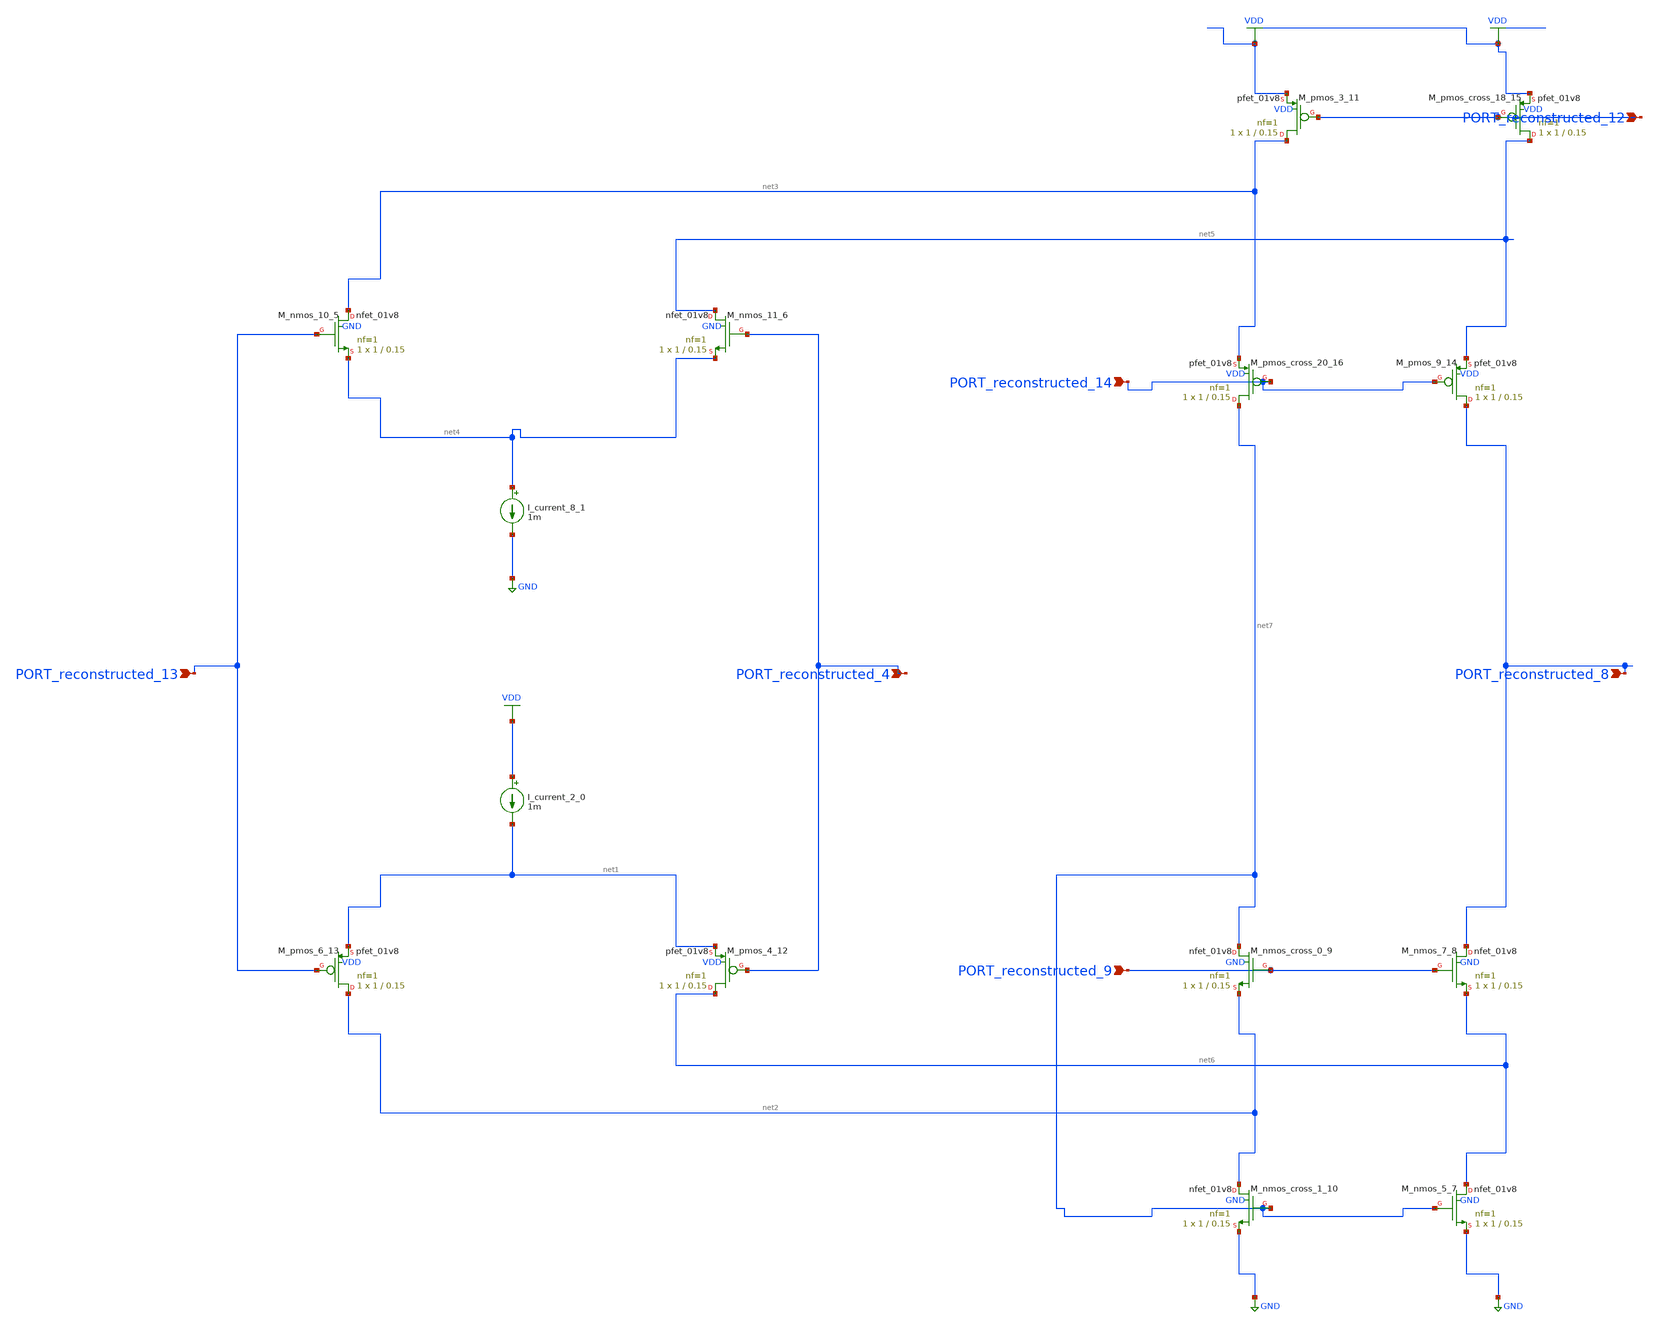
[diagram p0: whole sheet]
** sch_path: schematics/AMSNet/684.sch
**.subckt 684 PORT_reconstructed_4 PORT_reconstructed_8 PORT_reconstructed_13 PORT_reconstructed_9
*+ PORT_reconstructed_14 PORT_reconstructed_12
*.ipin PORT_reconstructed_4
*.ipin PORT_reconstructed_8
*.ipin PORT_reconstructed_13
*.ipin PORT_reconstructed_9
*.ipin PORT_reconstructed_14
*.ipin PORT_reconstructed_12
I_current_2_0 VDD net1 1m
I_current_8_1 net4 GND 1m
XM_nmos_10_5 net3 PORT_reconstructed_13 net4 GND sky130_fd_pr__nfet_01v8 L=0.15 W=1 nf=1 ad='int((1 + 1)/2) * 1 / 1 * 0.29'
+ as='int((1 + 2)/2) * 1 / 1 * 0.29' pd='2*int((1 + 1)/2) * (1 / 1 + 0.29)' ps='2*int((1 + 2)/2) * (1 / 1 + 0.29)'
+ nrd='0.29 / 1 ' nrs='0.29 / 1 ' sa=0 sb=0 sd=0 mult=1 m=1
XM_nmos_11_6 net5 PORT_reconstructed_4 net4 GND sky130_fd_pr__nfet_01v8 L=0.15 W=1 nf=1 ad='int((1 + 1)/2) * 1 / 1 * 0.29'
+ as='int((1 + 2)/2) * 1 / 1 * 0.29' pd='2*int((1 + 1)/2) * (1 / 1 + 0.29)' ps='2*int((1 + 2)/2) * (1 / 1 + 0.29)'
+ nrd='0.29 / 1 ' nrs='0.29 / 1 ' sa=0 sb=0 sd=0 mult=1 m=1
XM_nmos_5_7 net6 net7 GND GND sky130_fd_pr__nfet_01v8 L=0.15 W=1 nf=1 ad='int((1 + 1)/2) * 1 / 1 * 0.29'
+ as='int((1 + 2)/2) * 1 / 1 * 0.29' pd='2*int((1 + 1)/2) * (1 / 1 + 0.29)' ps='2*int((1 + 2)/2) * (1 / 1 + 0.29)'
+ nrd='0.29 / 1 ' nrs='0.29 / 1 ' sa=0 sb=0 sd=0 mult=1 m=1
XM_nmos_7_8 PORT_reconstructed_8 PORT_reconstructed_9 net6 GND sky130_fd_pr__nfet_01v8 L=0.15 W=1 nf=1
+ ad='int((1 + 1)/2) * 1 / 1 * 0.29' as='int((1 + 2)/2) * 1 / 1 * 0.29' pd='2*int((1 + 1)/2) * (1 / 1 + 0.29)'
+ ps='2*int((1 + 2)/2) * (1 / 1 + 0.29)' nrd='0.29 / 1 ' nrs='0.29 / 1 ' sa=0 sb=0 sd=0 mult=1 m=1
XM_nmos_cross_0_9 net7 PORT_reconstructed_9 net2 GND sky130_fd_pr__nfet_01v8 L=0.15 W=1 nf=1 ad='int((1 + 1)/2) * 1 / 1 * 0.29'
+ as='int((1 + 2)/2) * 1 / 1 * 0.29' pd='2*int((1 + 1)/2) * (1 / 1 + 0.29)' ps='2*int((1 + 2)/2) * (1 / 1 + 0.29)'
+ nrd='0.29 / 1 ' nrs='0.29 / 1 ' sa=0 sb=0 sd=0 mult=1 m=1
XM_nmos_cross_1_10 net2 net7 GND GND sky130_fd_pr__nfet_01v8 L=0.15 W=1 nf=1 ad='int((1 + 1)/2) * 1 / 1 * 0.29'
+ as='int((1 + 2)/2) * 1 / 1 * 0.29' pd='2*int((1 + 1)/2) * (1 / 1 + 0.29)' ps='2*int((1 + 2)/2) * (1 / 1 + 0.29)'
+ nrd='0.29 / 1 ' nrs='0.29 / 1 ' sa=0 sb=0 sd=0 mult=1 m=1
XM_pmos_3_11 net3 PORT_reconstructed_12 VDD VDD sky130_fd_pr__pfet_01v8 L=0.15 W=1 nf=1 ad='int((1 + 1)/2) * 1 / 1 * 0.29'
+ as='int((1 + 2)/2) * 1 / 1 * 0.29' pd='2*int((1 + 1)/2) * (1 / 1 + 0.29)' ps='2*int((1 + 2)/2) * (1 / 1 + 0.29)'
+ nrd='0.29 / 1 ' nrs='0.29 / 1 ' sa=0 sb=0 sd=0 mult=1 m=1
XM_pmos_4_12 net6 PORT_reconstructed_4 net1 VDD sky130_fd_pr__pfet_01v8 L=0.15 W=1 nf=1 ad='int((1 + 1)/2) * 1 / 1 * 0.29'
+ as='int((1 + 2)/2) * 1 / 1 * 0.29' pd='2*int((1 + 1)/2) * (1 / 1 + 0.29)' ps='2*int((1 + 2)/2) * (1 / 1 + 0.29)'
+ nrd='0.29 / 1 ' nrs='0.29 / 1 ' sa=0 sb=0 sd=0 mult=1 m=1
XM_pmos_6_13 net2 PORT_reconstructed_13 net1 VDD sky130_fd_pr__pfet_01v8 L=0.15 W=1 nf=1 ad='int((1 + 1)/2) * 1 / 1 * 0.29'
+ as='int((1 + 2)/2) * 1 / 1 * 0.29' pd='2*int((1 + 1)/2) * (1 / 1 + 0.29)' ps='2*int((1 + 2)/2) * (1 / 1 + 0.29)'
+ nrd='0.29 / 1 ' nrs='0.29 / 1 ' sa=0 sb=0 sd=0 mult=1 m=1
XM_pmos_9_14 PORT_reconstructed_8 PORT_reconstructed_14 net5 VDD sky130_fd_pr__pfet_01v8 L=0.15 W=1 nf=1
+ ad='int((1 + 1)/2) * 1 / 1 * 0.29' as='int((1 + 2)/2) * 1 / 1 * 0.29' pd='2*int((1 + 1)/2) * (1 / 1 + 0.29)'
+ ps='2*int((1 + 2)/2) * (1 / 1 + 0.29)' nrd='0.29 / 1 ' nrs='0.29 / 1 ' sa=0 sb=0 sd=0 mult=1 m=1
XM_pmos_cross_18_15 net5 PORT_reconstructed_12 VDD VDD sky130_fd_pr__pfet_01v8 L=0.15 W=1 nf=1 ad='int((1 + 1)/2) * 1 / 1 * 0.29'
+ as='int((1 + 2)/2) * 1 / 1 * 0.29' pd='2*int((1 + 1)/2) * (1 / 1 + 0.29)' ps='2*int((1 + 2)/2) * (1 / 1 + 0.29)'
+ nrd='0.29 / 1 ' nrs='0.29 / 1 ' sa=0 sb=0 sd=0 mult=1 m=1
XM_pmos_cross_20_16 net7 PORT_reconstructed_14 net3 VDD sky130_fd_pr__pfet_01v8 L=0.15 W=1 nf=1 ad='int((1 + 1)/2) * 1 / 1 * 0.29'
+ as='int((1 + 2)/2) * 1 / 1 * 0.29' pd='2*int((1 + 1)/2) * (1 / 1 + 0.29)' ps='2*int((1 + 2)/2) * (1 / 1 + 0.29)'
+ nrd='0.29 / 1 ' nrs='0.29 / 1 ' sa=0 sb=0 sd=0 mult=1 m=1
**.ends
.GLOBAL GND
.GLOBAL VDD
.end
